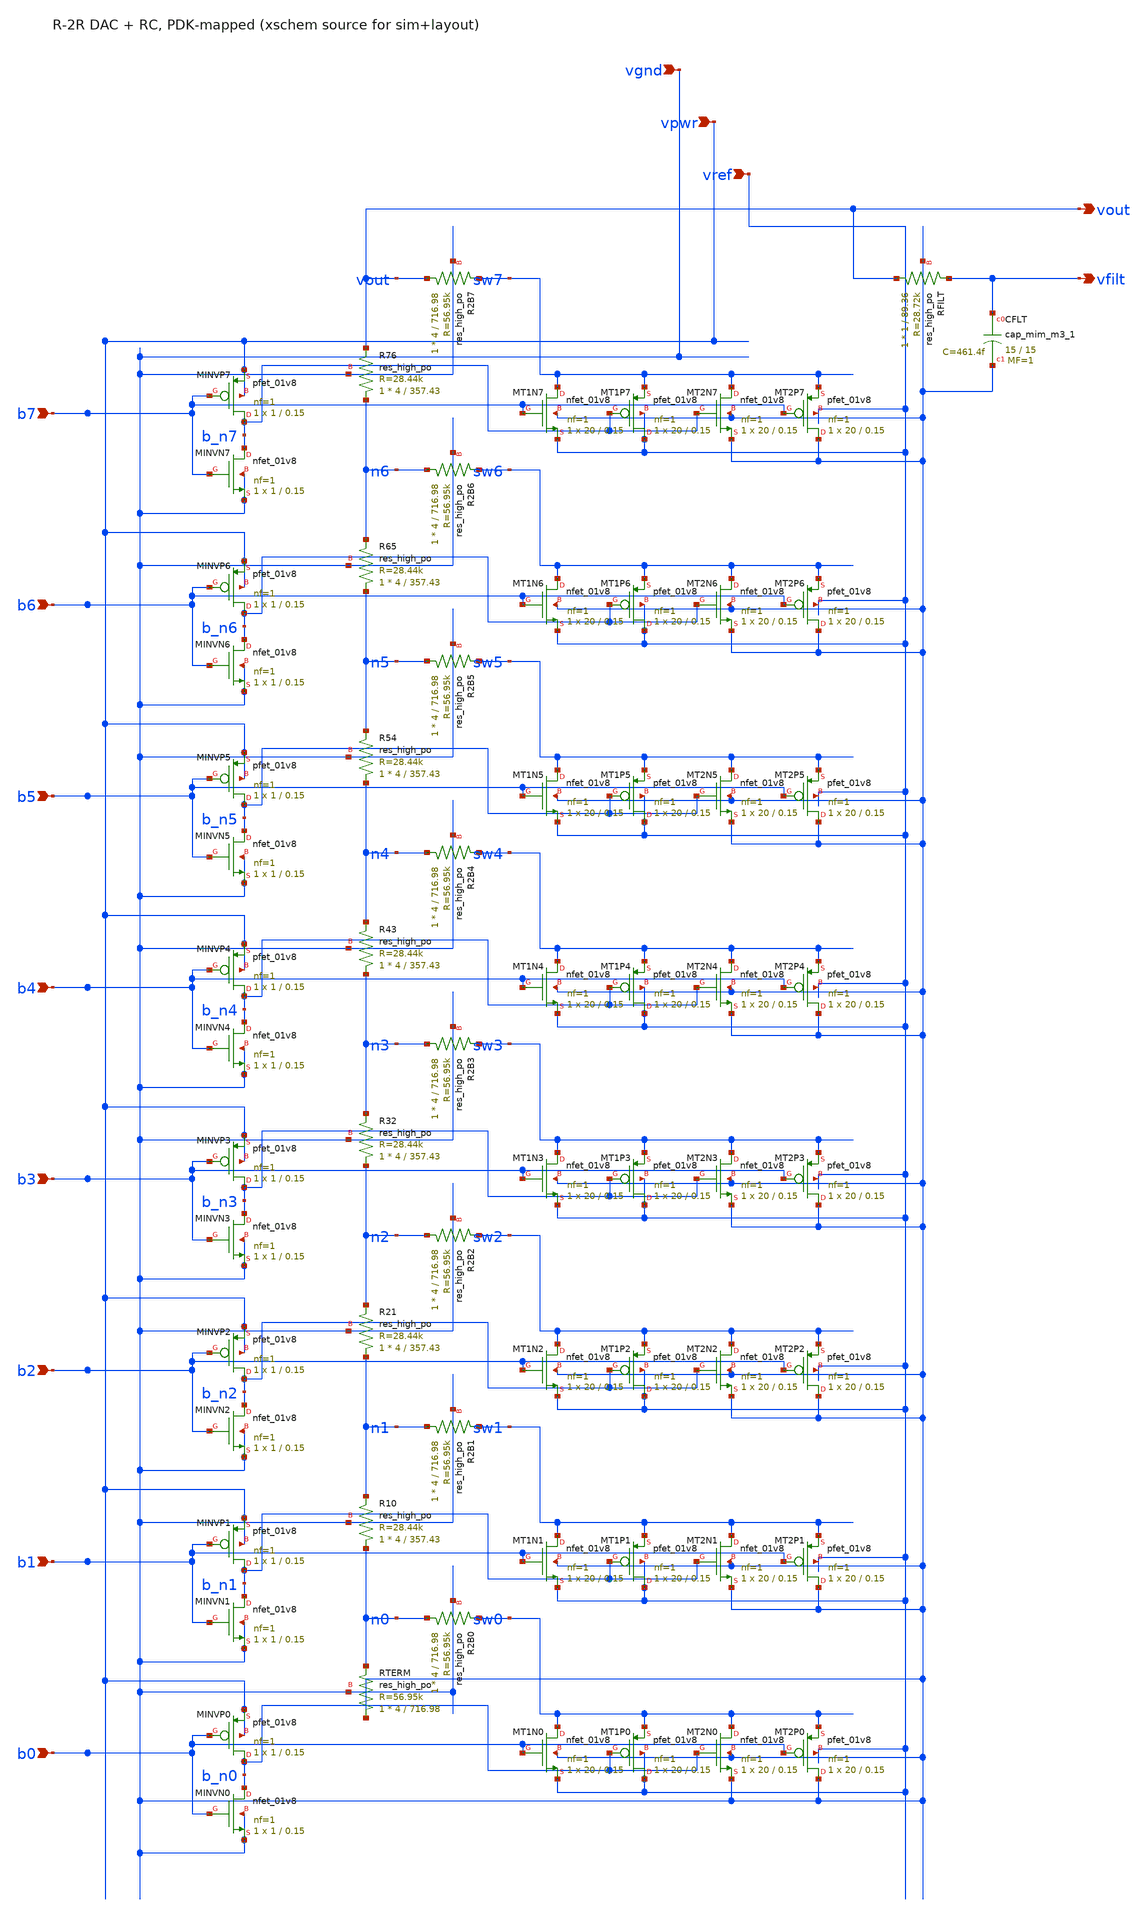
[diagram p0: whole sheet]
** sch_path: design/analog/xschem/r2r_dac8_pdk.sch
**.subckt r2r_dac8_pdk b7 b6 b5 b4 b3 b2 b1 b0 vref vpwr vgnd vfilt vout
*.ipin b7
*.ipin b6
*.ipin b5
*.ipin b4
*.ipin b3
*.ipin b2
*.ipin b1
*.ipin b0
*.ipin vref
*.ipin vpwr
*.ipin vgnd
*.opin vfilt
*.opin vout
XR76 n6 vout vgnd sky130_fd_pr__res_high_po W=4 L=357.43 mult=1 m=1
XR65 n5 n6 vgnd sky130_fd_pr__res_high_po W=4 L=357.43 mult=1 m=1
XR54 n4 n5 vgnd sky130_fd_pr__res_high_po W=4 L=357.43 mult=1 m=1
XR43 n3 n4 vgnd sky130_fd_pr__res_high_po W=4 L=357.43 mult=1 m=1
XR32 n2 n3 vgnd sky130_fd_pr__res_high_po W=4 L=357.43 mult=1 m=1
XR21 n1 n2 vgnd sky130_fd_pr__res_high_po W=4 L=357.43 mult=1 m=1
XR10 n0 n1 vgnd sky130_fd_pr__res_high_po W=4 L=357.43 mult=1 m=1
XRTERM vgnd n0 vgnd sky130_fd_pr__res_high_po W=4 L=716.98 mult=1 m=1
XR2B7 vout sw7 vgnd sky130_fd_pr__res_high_po W=4 L=716.98 mult=1 m=1
XMT1N7 sw7 b7 vref vgnd sky130_fd_pr__nfet_01v8 L=0.15 W=20 nf=1 ad='int((1 + 1)/2) * 20 / 1 * 0.29'
+ as='int((1 + 2)/2) * 20 / 1 * 0.29' pd='2*int((1 + 1)/2) * (20 / 1 + 0.29)' ps='2*int((1 + 2)/2) * (20 / 1 + 0.29)'
+ nrd='0.29 / 20 ' nrs='0.29 / 20 ' sa=0 sb=0 sd=0 mult=1 m=1
XMT1P7 vref b_n7 sw7 vref sky130_fd_pr__pfet_01v8 L=0.15 W=20 nf=1 ad='int((nf+1)/2) * W/nf * 0.29' as='int((nf+2)/2) * W/nf * 0.29'
+ pd='2*int((nf+1)/2) * (W/nf + 0.29)' ps='2*int((nf+2)/2) * (W/nf + 0.29)' nrd='0.29 / W' nrs='0.29 / W'
+ sa=0 sb=0 sd=0 mult=1 m=1
XMT2N7 sw7 b_n7 vgnd vgnd sky130_fd_pr__nfet_01v8 L=0.15 W=20 nf=1 ad='int((1 + 1)/2) * 20 / 1 * 0.29'
+ as='int((1 + 2)/2) * 20 / 1 * 0.29' pd='2*int((1 + 1)/2) * (20 / 1 + 0.29)' ps='2*int((1 + 2)/2) * (20 / 1 + 0.29)'
+ nrd='0.29 / 20 ' nrs='0.29 / 20 ' sa=0 sb=0 sd=0 mult=1 m=1
XMT2P7 vgnd b7 sw7 vref sky130_fd_pr__pfet_01v8 L=0.15 W=20 nf=1 ad='int((nf+1)/2) * W/nf * 0.29' as='int((nf+2)/2) * W/nf * 0.29'
+ pd='2*int((nf+1)/2) * (W/nf + 0.29)' ps='2*int((nf+2)/2) * (W/nf + 0.29)' nrd='0.29 / W' nrs='0.29 / W'
+ sa=0 sb=0 sd=0 mult=1 m=1
XMINVP7 b_n7 b7 vpwr vpwr sky130_fd_pr__pfet_01v8 L=0.15 W=1 nf=1 ad='int((nf+1)/2) * W/nf * 0.29' as='int((nf+2)/2) * W/nf * 0.29'
+ pd='2*int((nf+1)/2) * (W/nf + 0.29)' ps='2*int((nf+2)/2) * (W/nf + 0.29)' nrd='0.29 / W' nrs='0.29 / W'
+ sa=0 sb=0 sd=0 mult=1 m=1
XMINVN7 b_n7 b7 vgnd vgnd sky130_fd_pr__nfet_01v8 L=0.15 W=1 nf=1 ad='int((1 + 1)/2) * 1 / 1 * 0.29'
+ as='int((1 + 2)/2) * 1 / 1 * 0.29' pd='2*int((1 + 1)/2) * (1 / 1 + 0.29)' ps='2*int((1 + 2)/2) * (1 / 1 + 0.29)'
+ nrd='0.29 / 1 ' nrs='0.29 / 1 ' sa=0 sb=0 sd=0 mult=1 m=1
XR2B6 n6 sw6 vgnd sky130_fd_pr__res_high_po W=4 L=716.98 mult=1 m=1
XMT1N6 sw6 b6 vref vgnd sky130_fd_pr__nfet_01v8 L=0.15 W=20 nf=1 ad='int((1 + 1)/2) * 20 / 1 * 0.29'
+ as='int((1 + 2)/2) * 20 / 1 * 0.29' pd='2*int((1 + 1)/2) * (20 / 1 + 0.29)' ps='2*int((1 + 2)/2) * (20 / 1 + 0.29)'
+ nrd='0.29 / 20 ' nrs='0.29 / 20 ' sa=0 sb=0 sd=0 mult=1 m=1
XMT1P6 vref b_n6 sw6 vref sky130_fd_pr__pfet_01v8 L=0.15 W=20 nf=1 ad='int((nf+1)/2) * W/nf * 0.29' as='int((nf+2)/2) * W/nf * 0.29'
+ pd='2*int((nf+1)/2) * (W/nf + 0.29)' ps='2*int((nf+2)/2) * (W/nf + 0.29)' nrd='0.29 / W' nrs='0.29 / W'
+ sa=0 sb=0 sd=0 mult=1 m=1
XMT2N6 sw6 b_n6 vgnd vgnd sky130_fd_pr__nfet_01v8 L=0.15 W=20 nf=1 ad='int((1 + 1)/2) * 20 / 1 * 0.29'
+ as='int((1 + 2)/2) * 20 / 1 * 0.29' pd='2*int((1 + 1)/2) * (20 / 1 + 0.29)' ps='2*int((1 + 2)/2) * (20 / 1 + 0.29)'
+ nrd='0.29 / 20 ' nrs='0.29 / 20 ' sa=0 sb=0 sd=0 mult=1 m=1
XMT2P6 vgnd b6 sw6 vref sky130_fd_pr__pfet_01v8 L=0.15 W=20 nf=1 ad='int((nf+1)/2) * W/nf * 0.29' as='int((nf+2)/2) * W/nf * 0.29'
+ pd='2*int((nf+1)/2) * (W/nf + 0.29)' ps='2*int((nf+2)/2) * (W/nf + 0.29)' nrd='0.29 / W' nrs='0.29 / W'
+ sa=0 sb=0 sd=0 mult=1 m=1
XMINVP6 b_n6 b6 vpwr vpwr sky130_fd_pr__pfet_01v8 L=0.15 W=1 nf=1 ad='int((nf+1)/2) * W/nf * 0.29' as='int((nf+2)/2) * W/nf * 0.29'
+ pd='2*int((nf+1)/2) * (W/nf + 0.29)' ps='2*int((nf+2)/2) * (W/nf + 0.29)' nrd='0.29 / W' nrs='0.29 / W'
+ sa=0 sb=0 sd=0 mult=1 m=1
XMINVN6 b_n6 b6 vgnd vgnd sky130_fd_pr__nfet_01v8 L=0.15 W=1 nf=1 ad='int((1 + 1)/2) * 1 / 1 * 0.29'
+ as='int((1 + 2)/2) * 1 / 1 * 0.29' pd='2*int((1 + 1)/2) * (1 / 1 + 0.29)' ps='2*int((1 + 2)/2) * (1 / 1 + 0.29)'
+ nrd='0.29 / 1 ' nrs='0.29 / 1 ' sa=0 sb=0 sd=0 mult=1 m=1
XR2B5 n5 sw5 vgnd sky130_fd_pr__res_high_po W=4 L=716.98 mult=1 m=1
XMT1N5 sw5 b5 vref vgnd sky130_fd_pr__nfet_01v8 L=0.15 W=20 nf=1 ad='int((1 + 1)/2) * 20 / 1 * 0.29'
+ as='int((1 + 2)/2) * 20 / 1 * 0.29' pd='2*int((1 + 1)/2) * (20 / 1 + 0.29)' ps='2*int((1 + 2)/2) * (20 / 1 + 0.29)'
+ nrd='0.29 / 20 ' nrs='0.29 / 20 ' sa=0 sb=0 sd=0 mult=1 m=1
XMT1P5 vref b_n5 sw5 vref sky130_fd_pr__pfet_01v8 L=0.15 W=20 nf=1 ad='int((nf+1)/2) * W/nf * 0.29' as='int((nf+2)/2) * W/nf * 0.29'
+ pd='2*int((nf+1)/2) * (W/nf + 0.29)' ps='2*int((nf+2)/2) * (W/nf + 0.29)' nrd='0.29 / W' nrs='0.29 / W'
+ sa=0 sb=0 sd=0 mult=1 m=1
XMT2N5 sw5 b_n5 vgnd vgnd sky130_fd_pr__nfet_01v8 L=0.15 W=20 nf=1 ad='int((1 + 1)/2) * 20 / 1 * 0.29'
+ as='int((1 + 2)/2) * 20 / 1 * 0.29' pd='2*int((1 + 1)/2) * (20 / 1 + 0.29)' ps='2*int((1 + 2)/2) * (20 / 1 + 0.29)'
+ nrd='0.29 / 20 ' nrs='0.29 / 20 ' sa=0 sb=0 sd=0 mult=1 m=1
XMT2P5 vgnd b5 sw5 vref sky130_fd_pr__pfet_01v8 L=0.15 W=20 nf=1 ad='int((nf+1)/2) * W/nf * 0.29' as='int((nf+2)/2) * W/nf * 0.29'
+ pd='2*int((nf+1)/2) * (W/nf + 0.29)' ps='2*int((nf+2)/2) * (W/nf + 0.29)' nrd='0.29 / W' nrs='0.29 / W'
+ sa=0 sb=0 sd=0 mult=1 m=1
XMINVP5 b_n5 b5 vpwr vpwr sky130_fd_pr__pfet_01v8 L=0.15 W=1 nf=1 ad='int((nf+1)/2) * W/nf * 0.29' as='int((nf+2)/2) * W/nf * 0.29'
+ pd='2*int((nf+1)/2) * (W/nf + 0.29)' ps='2*int((nf+2)/2) * (W/nf + 0.29)' nrd='0.29 / W' nrs='0.29 / W'
+ sa=0 sb=0 sd=0 mult=1 m=1
XMINVN5 b_n5 b5 vgnd vgnd sky130_fd_pr__nfet_01v8 L=0.15 W=1 nf=1 ad='int((1 + 1)/2) * 1 / 1 * 0.29'
+ as='int((1 + 2)/2) * 1 / 1 * 0.29' pd='2*int((1 + 1)/2) * (1 / 1 + 0.29)' ps='2*int((1 + 2)/2) * (1 / 1 + 0.29)'
+ nrd='0.29 / 1 ' nrs='0.29 / 1 ' sa=0 sb=0 sd=0 mult=1 m=1
XR2B4 n4 sw4 vgnd sky130_fd_pr__res_high_po W=4 L=716.98 mult=1 m=1
XMT1N4 sw4 b4 vref vgnd sky130_fd_pr__nfet_01v8 L=0.15 W=20 nf=1 ad='int((1 + 1)/2) * 20 / 1 * 0.29'
+ as='int((1 + 2)/2) * 20 / 1 * 0.29' pd='2*int((1 + 1)/2) * (20 / 1 + 0.29)' ps='2*int((1 + 2)/2) * (20 / 1 + 0.29)'
+ nrd='0.29 / 20 ' nrs='0.29 / 20 ' sa=0 sb=0 sd=0 mult=1 m=1
XMT1P4 vref b_n4 sw4 vref sky130_fd_pr__pfet_01v8 L=0.15 W=20 nf=1 ad='int((nf+1)/2) * W/nf * 0.29' as='int((nf+2)/2) * W/nf * 0.29'
+ pd='2*int((nf+1)/2) * (W/nf + 0.29)' ps='2*int((nf+2)/2) * (W/nf + 0.29)' nrd='0.29 / W' nrs='0.29 / W'
+ sa=0 sb=0 sd=0 mult=1 m=1
XMT2N4 sw4 b_n4 vgnd vgnd sky130_fd_pr__nfet_01v8 L=0.15 W=20 nf=1 ad='int((1 + 1)/2) * 20 / 1 * 0.29'
+ as='int((1 + 2)/2) * 20 / 1 * 0.29' pd='2*int((1 + 1)/2) * (20 / 1 + 0.29)' ps='2*int((1 + 2)/2) * (20 / 1 + 0.29)'
+ nrd='0.29 / 20 ' nrs='0.29 / 20 ' sa=0 sb=0 sd=0 mult=1 m=1
XMT2P4 vgnd b4 sw4 vref sky130_fd_pr__pfet_01v8 L=0.15 W=20 nf=1 ad='int((nf+1)/2) * W/nf * 0.29' as='int((nf+2)/2) * W/nf * 0.29'
+ pd='2*int((nf+1)/2) * (W/nf + 0.29)' ps='2*int((nf+2)/2) * (W/nf + 0.29)' nrd='0.29 / W' nrs='0.29 / W'
+ sa=0 sb=0 sd=0 mult=1 m=1
XMINVP4 b_n4 b4 vpwr vpwr sky130_fd_pr__pfet_01v8 L=0.15 W=1 nf=1 ad='int((nf+1)/2) * W/nf * 0.29' as='int((nf+2)/2) * W/nf * 0.29'
+ pd='2*int((nf+1)/2) * (W/nf + 0.29)' ps='2*int((nf+2)/2) * (W/nf + 0.29)' nrd='0.29 / W' nrs='0.29 / W'
+ sa=0 sb=0 sd=0 mult=1 m=1
XMINVN4 b_n4 b4 vgnd vgnd sky130_fd_pr__nfet_01v8 L=0.15 W=1 nf=1 ad='int((1 + 1)/2) * 1 / 1 * 0.29'
+ as='int((1 + 2)/2) * 1 / 1 * 0.29' pd='2*int((1 + 1)/2) * (1 / 1 + 0.29)' ps='2*int((1 + 2)/2) * (1 / 1 + 0.29)'
+ nrd='0.29 / 1 ' nrs='0.29 / 1 ' sa=0 sb=0 sd=0 mult=1 m=1
XR2B3 n3 sw3 vgnd sky130_fd_pr__res_high_po W=4 L=716.98 mult=1 m=1
XMT1N3 sw3 b3 vref vgnd sky130_fd_pr__nfet_01v8 L=0.15 W=20 nf=1 ad='int((1 + 1)/2) * 20 / 1 * 0.29'
+ as='int((1 + 2)/2) * 20 / 1 * 0.29' pd='2*int((1 + 1)/2) * (20 / 1 + 0.29)' ps='2*int((1 + 2)/2) * (20 / 1 + 0.29)'
+ nrd='0.29 / 20 ' nrs='0.29 / 20 ' sa=0 sb=0 sd=0 mult=1 m=1
XMT1P3 vref b_n3 sw3 vref sky130_fd_pr__pfet_01v8 L=0.15 W=20 nf=1 ad='int((nf+1)/2) * W/nf * 0.29' as='int((nf+2)/2) * W/nf * 0.29'
+ pd='2*int((nf+1)/2) * (W/nf + 0.29)' ps='2*int((nf+2)/2) * (W/nf + 0.29)' nrd='0.29 / W' nrs='0.29 / W'
+ sa=0 sb=0 sd=0 mult=1 m=1
XMT2N3 sw3 b_n3 vgnd vgnd sky130_fd_pr__nfet_01v8 L=0.15 W=20 nf=1 ad='int((1 + 1)/2) * 20 / 1 * 0.29'
+ as='int((1 + 2)/2) * 20 / 1 * 0.29' pd='2*int((1 + 1)/2) * (20 / 1 + 0.29)' ps='2*int((1 + 2)/2) * (20 / 1 + 0.29)'
+ nrd='0.29 / 20 ' nrs='0.29 / 20 ' sa=0 sb=0 sd=0 mult=1 m=1
XMT2P3 vgnd b3 sw3 vref sky130_fd_pr__pfet_01v8 L=0.15 W=20 nf=1 ad='int((nf+1)/2) * W/nf * 0.29' as='int((nf+2)/2) * W/nf * 0.29'
+ pd='2*int((nf+1)/2) * (W/nf + 0.29)' ps='2*int((nf+2)/2) * (W/nf + 0.29)' nrd='0.29 / W' nrs='0.29 / W'
+ sa=0 sb=0 sd=0 mult=1 m=1
XMINVP3 b_n3 b3 vpwr vpwr sky130_fd_pr__pfet_01v8 L=0.15 W=1 nf=1 ad='int((nf+1)/2) * W/nf * 0.29' as='int((nf+2)/2) * W/nf * 0.29'
+ pd='2*int((nf+1)/2) * (W/nf + 0.29)' ps='2*int((nf+2)/2) * (W/nf + 0.29)' nrd='0.29 / W' nrs='0.29 / W'
+ sa=0 sb=0 sd=0 mult=1 m=1
XMINVN3 b_n3 b3 vgnd vgnd sky130_fd_pr__nfet_01v8 L=0.15 W=1 nf=1 ad='int((1 + 1)/2) * 1 / 1 * 0.29'
+ as='int((1 + 2)/2) * 1 / 1 * 0.29' pd='2*int((1 + 1)/2) * (1 / 1 + 0.29)' ps='2*int((1 + 2)/2) * (1 / 1 + 0.29)'
+ nrd='0.29 / 1 ' nrs='0.29 / 1 ' sa=0 sb=0 sd=0 mult=1 m=1
XR2B2 n2 sw2 vgnd sky130_fd_pr__res_high_po W=4 L=716.98 mult=1 m=1
XMT1N2 sw2 b2 vref vgnd sky130_fd_pr__nfet_01v8 L=0.15 W=20 nf=1 ad='int((1 + 1)/2) * 20 / 1 * 0.29'
+ as='int((1 + 2)/2) * 20 / 1 * 0.29' pd='2*int((1 + 1)/2) * (20 / 1 + 0.29)' ps='2*int((1 + 2)/2) * (20 / 1 + 0.29)'
+ nrd='0.29 / 20 ' nrs='0.29 / 20 ' sa=0 sb=0 sd=0 mult=1 m=1
XMT1P2 vref b_n2 sw2 vref sky130_fd_pr__pfet_01v8 L=0.15 W=20 nf=1 ad='int((nf+1)/2) * W/nf * 0.29' as='int((nf+2)/2) * W/nf * 0.29'
+ pd='2*int((nf+1)/2) * (W/nf + 0.29)' ps='2*int((nf+2)/2) * (W/nf + 0.29)' nrd='0.29 / W' nrs='0.29 / W'
+ sa=0 sb=0 sd=0 mult=1 m=1
XMT2N2 sw2 b_n2 vgnd vgnd sky130_fd_pr__nfet_01v8 L=0.15 W=20 nf=1 ad='int((1 + 1)/2) * 20 / 1 * 0.29'
+ as='int((1 + 2)/2) * 20 / 1 * 0.29' pd='2*int((1 + 1)/2) * (20 / 1 + 0.29)' ps='2*int((1 + 2)/2) * (20 / 1 + 0.29)'
+ nrd='0.29 / 20 ' nrs='0.29 / 20 ' sa=0 sb=0 sd=0 mult=1 m=1
XMT2P2 vgnd b2 sw2 vref sky130_fd_pr__pfet_01v8 L=0.15 W=20 nf=1 ad='int((nf+1)/2) * W/nf * 0.29' as='int((nf+2)/2) * W/nf * 0.29'
+ pd='2*int((nf+1)/2) * (W/nf + 0.29)' ps='2*int((nf+2)/2) * (W/nf + 0.29)' nrd='0.29 / W' nrs='0.29 / W'
+ sa=0 sb=0 sd=0 mult=1 m=1
XMINVP2 b_n2 b2 vpwr vpwr sky130_fd_pr__pfet_01v8 L=0.15 W=1 nf=1 ad='int((nf+1)/2) * W/nf * 0.29' as='int((nf+2)/2) * W/nf * 0.29'
+ pd='2*int((nf+1)/2) * (W/nf + 0.29)' ps='2*int((nf+2)/2) * (W/nf + 0.29)' nrd='0.29 / W' nrs='0.29 / W'
+ sa=0 sb=0 sd=0 mult=1 m=1
XMINVN2 b_n2 b2 vgnd vgnd sky130_fd_pr__nfet_01v8 L=0.15 W=1 nf=1 ad='int((1 + 1)/2) * 1 / 1 * 0.29'
+ as='int((1 + 2)/2) * 1 / 1 * 0.29' pd='2*int((1 + 1)/2) * (1 / 1 + 0.29)' ps='2*int((1 + 2)/2) * (1 / 1 + 0.29)'
+ nrd='0.29 / 1 ' nrs='0.29 / 1 ' sa=0 sb=0 sd=0 mult=1 m=1
XR2B1 n1 sw1 vgnd sky130_fd_pr__res_high_po W=4 L=716.98 mult=1 m=1
XMT1N1 sw1 b1 vref vgnd sky130_fd_pr__nfet_01v8 L=0.15 W=20 nf=1 ad='int((1 + 1)/2) * 20 / 1 * 0.29'
+ as='int((1 + 2)/2) * 20 / 1 * 0.29' pd='2*int((1 + 1)/2) * (20 / 1 + 0.29)' ps='2*int((1 + 2)/2) * (20 / 1 + 0.29)'
+ nrd='0.29 / 20 ' nrs='0.29 / 20 ' sa=0 sb=0 sd=0 mult=1 m=1
XMT1P1 vref b_n1 sw1 vref sky130_fd_pr__pfet_01v8 L=0.15 W=20 nf=1 ad='int((nf+1)/2) * W/nf * 0.29' as='int((nf+2)/2) * W/nf * 0.29'
+ pd='2*int((nf+1)/2) * (W/nf + 0.29)' ps='2*int((nf+2)/2) * (W/nf + 0.29)' nrd='0.29 / W' nrs='0.29 / W'
+ sa=0 sb=0 sd=0 mult=1 m=1
XMT2N1 sw1 b_n1 vgnd vgnd sky130_fd_pr__nfet_01v8 L=0.15 W=20 nf=1 ad='int((1 + 1)/2) * 20 / 1 * 0.29'
+ as='int((1 + 2)/2) * 20 / 1 * 0.29' pd='2*int((1 + 1)/2) * (20 / 1 + 0.29)' ps='2*int((1 + 2)/2) * (20 / 1 + 0.29)'
+ nrd='0.29 / 20 ' nrs='0.29 / 20 ' sa=0 sb=0 sd=0 mult=1 m=1
XMT2P1 vgnd b1 sw1 vref sky130_fd_pr__pfet_01v8 L=0.15 W=20 nf=1 ad='int((nf+1)/2) * W/nf * 0.29' as='int((nf+2)/2) * W/nf * 0.29'
+ pd='2*int((nf+1)/2) * (W/nf + 0.29)' ps='2*int((nf+2)/2) * (W/nf + 0.29)' nrd='0.29 / W' nrs='0.29 / W'
+ sa=0 sb=0 sd=0 mult=1 m=1
XMINVP1 b_n1 b1 vpwr vpwr sky130_fd_pr__pfet_01v8 L=0.15 W=1 nf=1 ad='int((nf+1)/2) * W/nf * 0.29' as='int((nf+2)/2) * W/nf * 0.29'
+ pd='2*int((nf+1)/2) * (W/nf + 0.29)' ps='2*int((nf+2)/2) * (W/nf + 0.29)' nrd='0.29 / W' nrs='0.29 / W'
+ sa=0 sb=0 sd=0 mult=1 m=1
XMINVN1 b_n1 b1 vgnd vgnd sky130_fd_pr__nfet_01v8 L=0.15 W=1 nf=1 ad='int((1 + 1)/2) * 1 / 1 * 0.29'
+ as='int((1 + 2)/2) * 1 / 1 * 0.29' pd='2*int((1 + 1)/2) * (1 / 1 + 0.29)' ps='2*int((1 + 2)/2) * (1 / 1 + 0.29)'
+ nrd='0.29 / 1 ' nrs='0.29 / 1 ' sa=0 sb=0 sd=0 mult=1 m=1
XR2B0 n0 sw0 vgnd sky130_fd_pr__res_high_po W=4 L=716.98 mult=1 m=1
XMT1N0 sw0 b0 vref vgnd sky130_fd_pr__nfet_01v8 L=0.15 W=20 nf=1 ad='int((1 + 1)/2) * 20 / 1 * 0.29'
+ as='int((1 + 2)/2) * 20 / 1 * 0.29' pd='2*int((1 + 1)/2) * (20 / 1 + 0.29)' ps='2*int((1 + 2)/2) * (20 / 1 + 0.29)'
+ nrd='0.29 / 20 ' nrs='0.29 / 20 ' sa=0 sb=0 sd=0 mult=1 m=1
XMT1P0 vref b_n0 sw0 vref sky130_fd_pr__pfet_01v8 L=0.15 W=20 nf=1 ad='int((nf+1)/2) * W/nf * 0.29' as='int((nf+2)/2) * W/nf * 0.29'
+ pd='2*int((nf+1)/2) * (W/nf + 0.29)' ps='2*int((nf+2)/2) * (W/nf + 0.29)' nrd='0.29 / W' nrs='0.29 / W'
+ sa=0 sb=0 sd=0 mult=1 m=1
XMT2N0 sw0 b_n0 vgnd vgnd sky130_fd_pr__nfet_01v8 L=0.15 W=20 nf=1 ad='int((1 + 1)/2) * 20 / 1 * 0.29'
+ as='int((1 + 2)/2) * 20 / 1 * 0.29' pd='2*int((1 + 1)/2) * (20 / 1 + 0.29)' ps='2*int((1 + 2)/2) * (20 / 1 + 0.29)'
+ nrd='0.29 / 20 ' nrs='0.29 / 20 ' sa=0 sb=0 sd=0 mult=1 m=1
XMT2P0 vgnd b0 sw0 vref sky130_fd_pr__pfet_01v8 L=0.15 W=20 nf=1 ad='int((nf+1)/2) * W/nf * 0.29' as='int((nf+2)/2) * W/nf * 0.29'
+ pd='2*int((nf+1)/2) * (W/nf + 0.29)' ps='2*int((nf+2)/2) * (W/nf + 0.29)' nrd='0.29 / W' nrs='0.29 / W'
+ sa=0 sb=0 sd=0 mult=1 m=1
XMINVP0 b_n0 b0 vpwr vpwr sky130_fd_pr__pfet_01v8 L=0.15 W=1 nf=1 ad='int((nf+1)/2) * W/nf * 0.29' as='int((nf+2)/2) * W/nf * 0.29'
+ pd='2*int((nf+1)/2) * (W/nf + 0.29)' ps='2*int((nf+2)/2) * (W/nf + 0.29)' nrd='0.29 / W' nrs='0.29 / W'
+ sa=0 sb=0 sd=0 mult=1 m=1
XMINVN0 b_n0 b0 vgnd vgnd sky130_fd_pr__nfet_01v8 L=0.15 W=1 nf=1 ad='int((1 + 1)/2) * 1 / 1 * 0.29'
+ as='int((1 + 2)/2) * 1 / 1 * 0.29' pd='2*int((1 + 1)/2) * (1 / 1 + 0.29)' ps='2*int((1 + 2)/2) * (1 / 1 + 0.29)'
+ nrd='0.29 / 1 ' nrs='0.29 / 1 ' sa=0 sb=0 sd=0 mult=1 m=1
XRFILT vout vfilt vgnd sky130_fd_pr__res_high_po W=1 L=89.36 mult=1 m=1
XCFLT vfilt vgnd sky130_fd_pr__cap_mim_m3_1 W=15 L=15 MF=1 m=1
**.ends
.end
